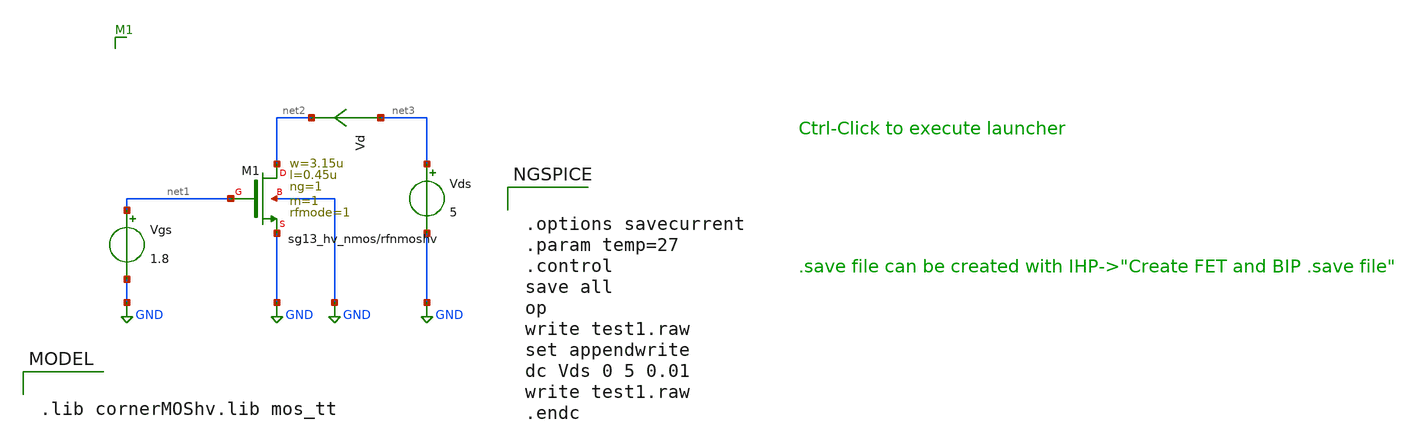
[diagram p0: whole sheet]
** sch_path: schematic/test1.sch
**.subckt test1
Vgs net1 GND 1.8
Vds net3 GND 5
Vd net3 net2 0
.save i(vd)
XM1 net2 net1 GND GND sg13_hv_nmos w=3.15u l=0.45u ng=1 m=1 rfmode=1 mm_ok=1
**** begin user architecture code

.lib cornerMOShv.lib mos_tt



.options savecurrent
.param temp=27
.control
save all
op
write test1.raw
set appendwrite
dc Vds 0 5 0.01
write test1.raw
.endc


**** end user architecture code
**.ends
.GLOBAL GND
.end
